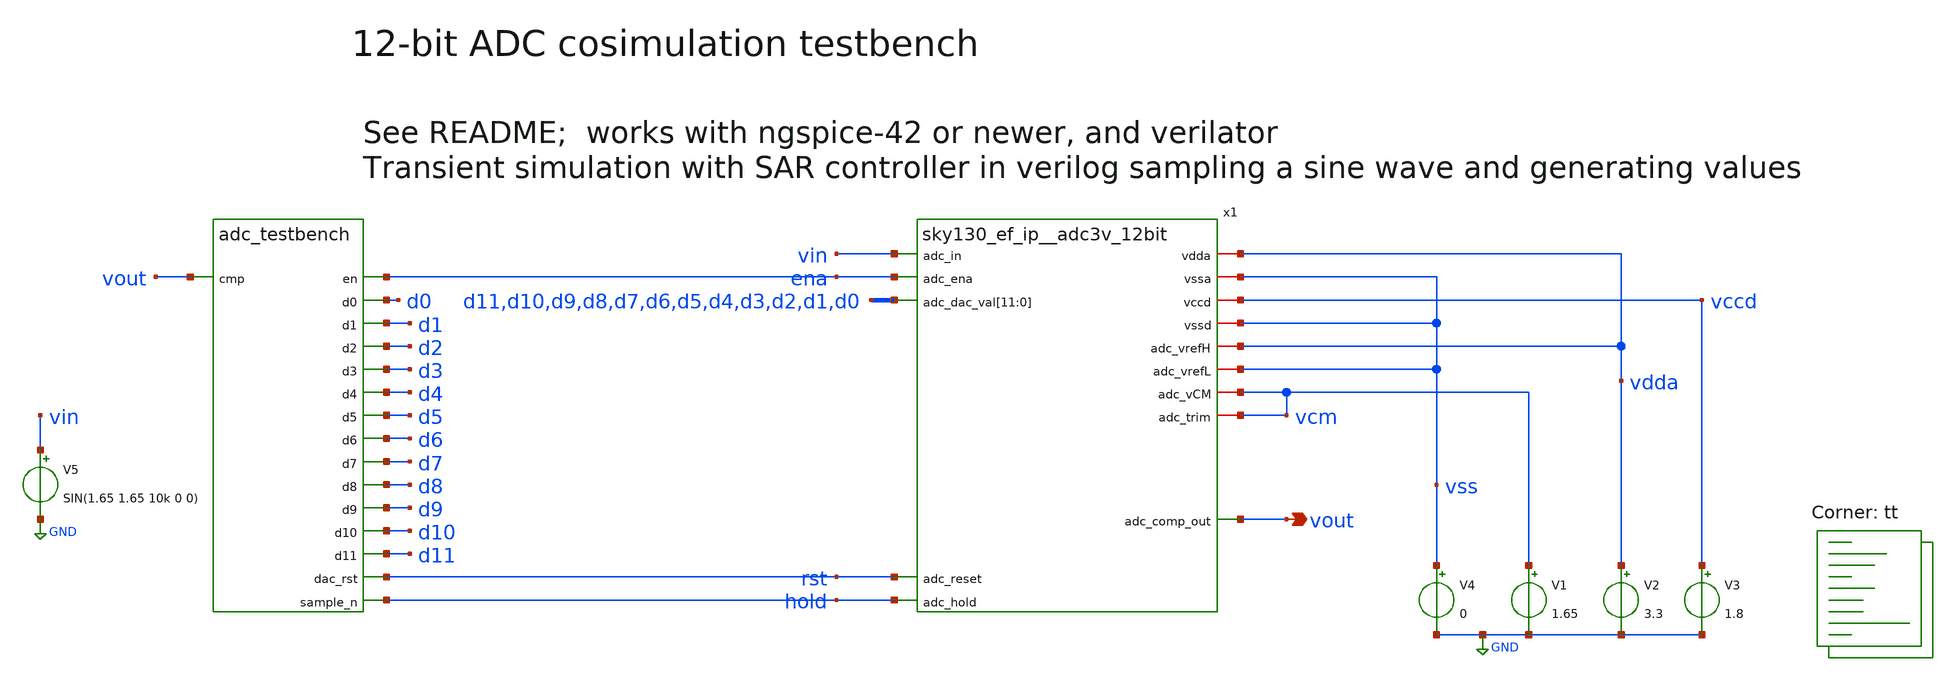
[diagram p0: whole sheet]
** sch_path: ip_references/adc/xschem/adc_cosim_tb.sch
**.subckt adc_cosim_tb vout
*.opin vout
x1 vdda vss vccd vss vdda vss vin ena d11 d10 d9 d8 d7 d6 d5 d4 d3 d2 d1 d0 vout rst vcm vcm hold
+ sky130_ef_ip__adc3v_12bit
V1 vcm GND 1.65
V2 vdda GND 3.3
V3 vccd GND 1.8
V4 vss GND 0
V5 vin GND SIN(1.65 1.65 10k 0 0)
asar [ vout ] [ ena rst hold d11 d10 d9 d8 d7 d6 d5 d4 d3 d2 d1 d0 ] null dut
.model dut d_cosim simulation="./adc_testbench.so"
**** begin user architecture code
.lib $::SKYWATER_MODELS/sky130.lib.spice tt

.include $PDK_ROOT/$PDK/libs.ref/sky130_fd_sc_hvl/spice/sky130_fd_sc_hvl.spice
.include $PDK_ROOT/$PDK/libs.ref/sky130_fd_sc_hd/spice/sky130_fd_sc_hd.spice
.control
   **save all
   save hold ena rst d11 d10 d9 d8 d7 d6 d5 d4 d3 d2 d1 d0
   save vin vout
   tran 1n 10.45u
   write simdata.raw
.endc


**** end user architecture code
**.ends
.GLOBAL GND
.end
